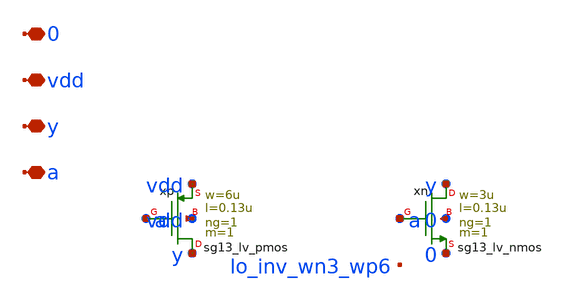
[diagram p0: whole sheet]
** sch_path: analog/lo/sch/lo_inv_3_6.sch
**.subckt lo_inv_3_6 a y vdd 0
*.iopin a
*.iopin y
*.iopin vdd
*.iopin 0
Xxp y a vdd vdd sg13_lv_pmos w=6u l=0.13u ng=1 m=1 mm_ok=1
Xxn y a 0 0 sg13_lv_nmos w=3u l=0.13u ng=1 m=1 mm_ok=1
**.ends
.end
